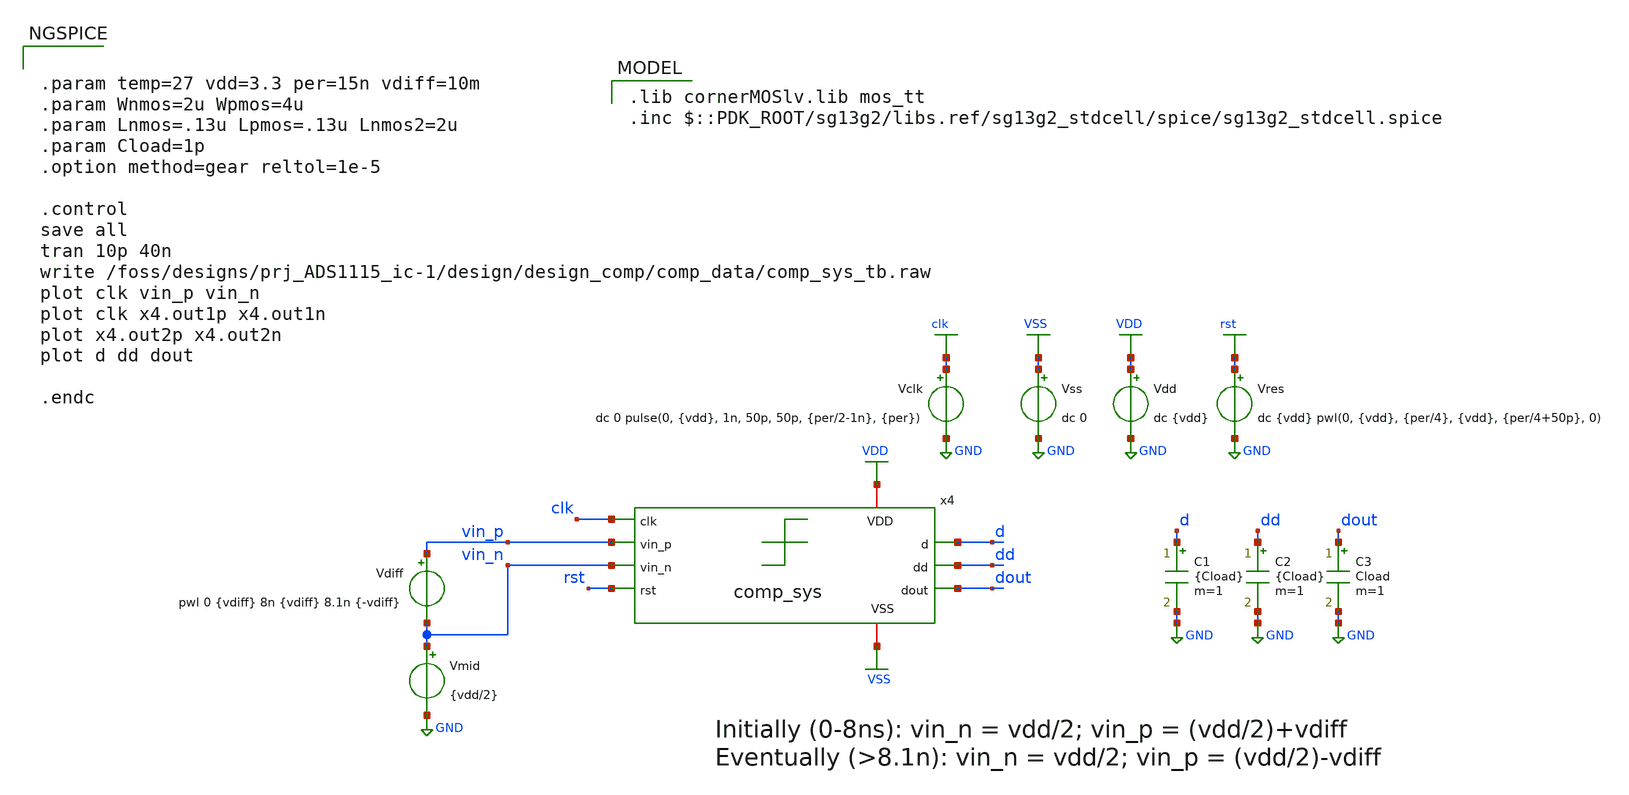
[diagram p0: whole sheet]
** sch_path: design/design_comp/tb_comp_sys_tran.sch
**.subckt tb_comp_sys_tran
Vdd VDD GND dc {vdd}
Vss VSS GND dc 0
Vdiff vin_p vin_n pwl 0 {vdiff} 8n {vdiff} 8.1n {-vdiff}
Vmid vin_n GND {vdd/2}
Vclk clk GND dc 0 pulse(0, {vdd}, 1n, 50p, 50p, {per/2-1n}, {per})
Vres rst GND dc {vdd} pwl(0, {vdd}, {per/4}, {vdd}, {per/4+50p}, 0)
x4 VDD clk d vin_p vin_n dd rst dout VSS comp_sys
C1 d GND {Cload} m=1
C2 dd GND {Cload} m=1
C3 dout GND Cload m=1
**** begin user architecture code


.param temp=27 vdd=3.3 per=15n vdiff=10m
.param Wnmos=2u Wpmos=4u
.param Lnmos=.13u Lpmos=.13u Lnmos2=2u
.param Cload=1p
.option method=gear reltol=1e-5

.control
save all
tran 10p 40n
write /foss/designs/prj_ADS1115_ic-1/design/design_comp/comp_data/comp_sys_tb.raw
plot clk vin_p vin_n
plot clk x4.out1p x4.out1n
plot x4.out2p x4.out2n
plot d dd dout

.endc

 .lib cornerMOSlv.lib mos_tt
.inc $::PDK_ROOT/sg13g2/libs.ref/sg13g2_stdcell/spice/sg13g2_stdcell.spice
**** end user architecture code
**.ends
.GLOBAL GND
.GLOBAL VDD
.GLOBAL VSS
.GLOBAL clk
.GLOBAL rst
.end
